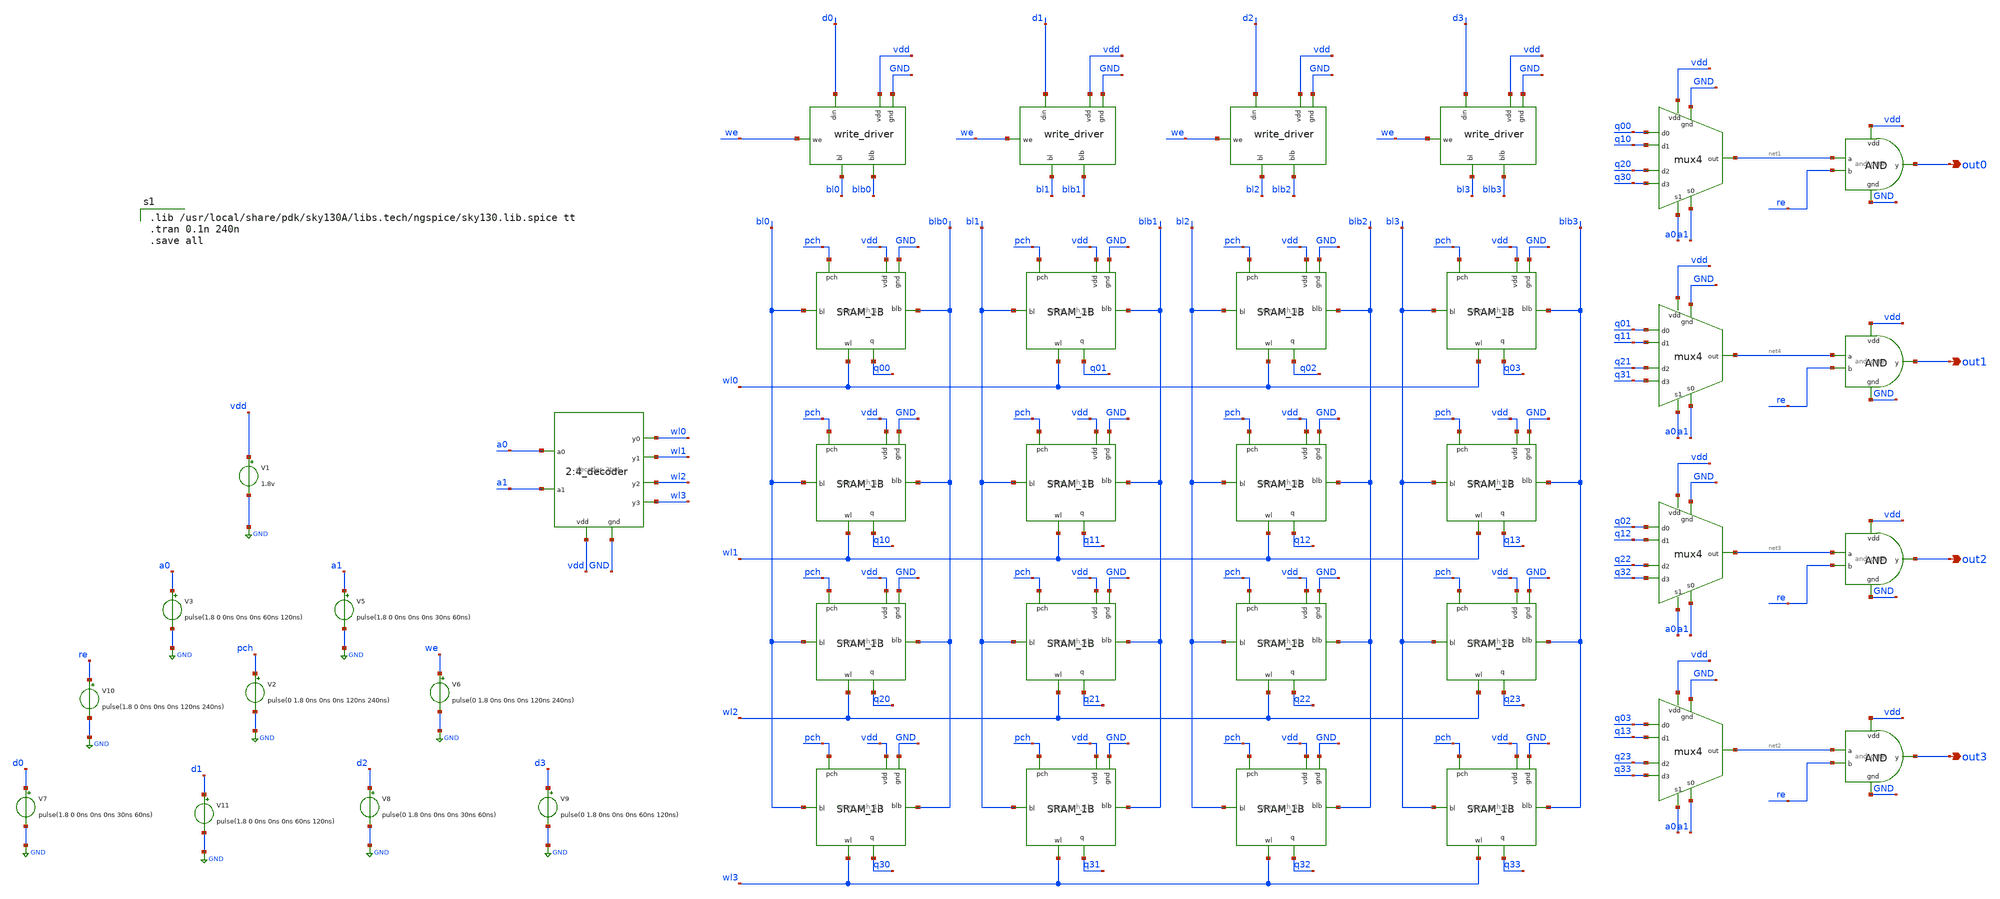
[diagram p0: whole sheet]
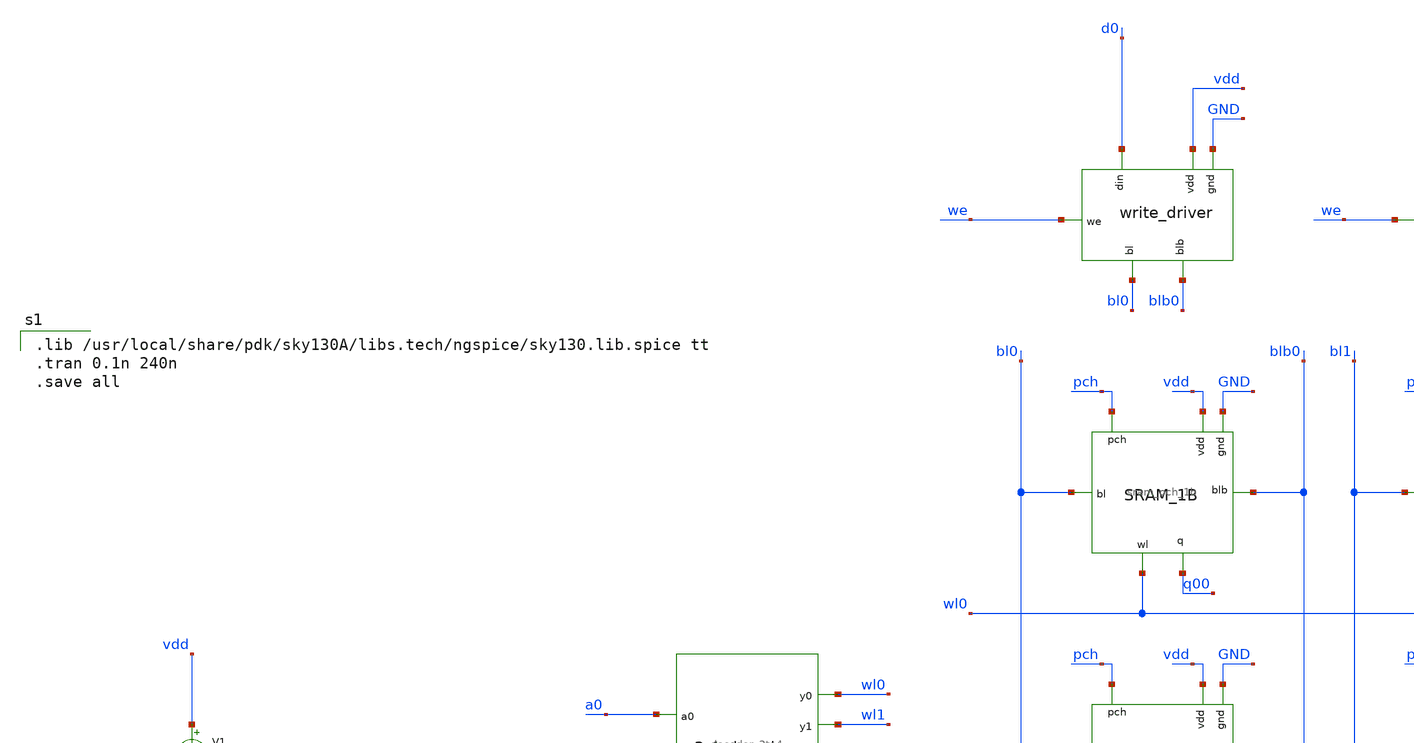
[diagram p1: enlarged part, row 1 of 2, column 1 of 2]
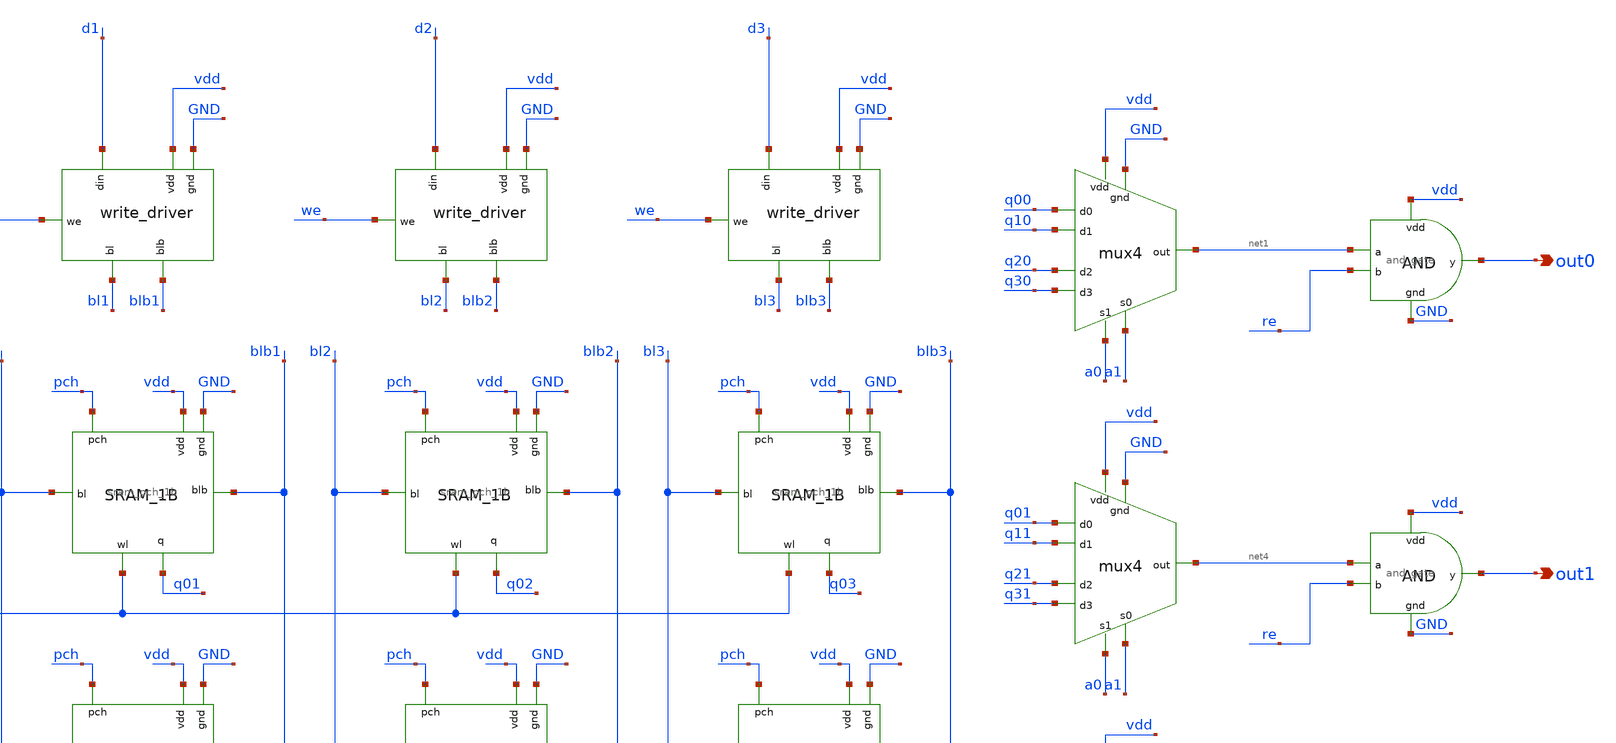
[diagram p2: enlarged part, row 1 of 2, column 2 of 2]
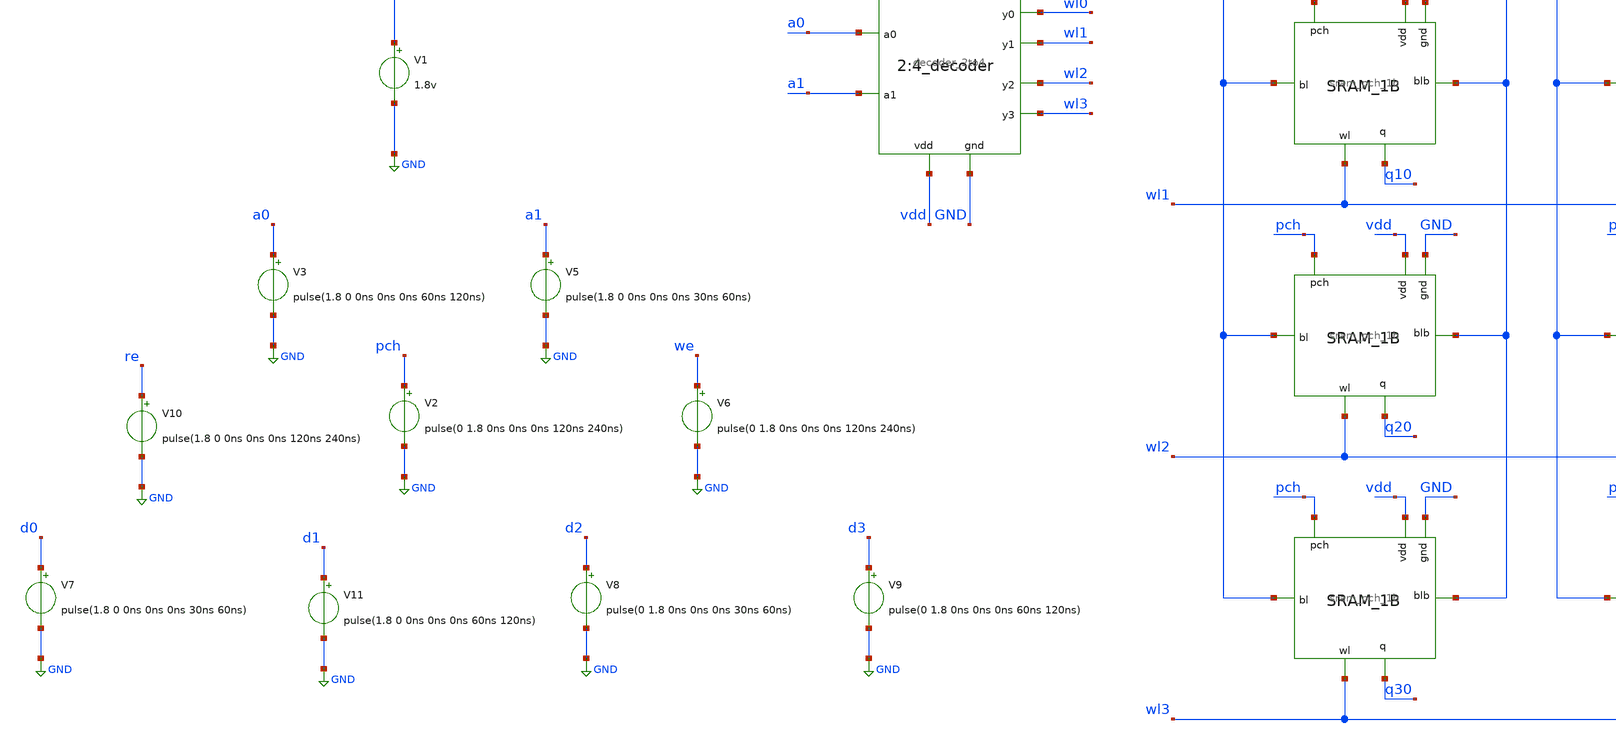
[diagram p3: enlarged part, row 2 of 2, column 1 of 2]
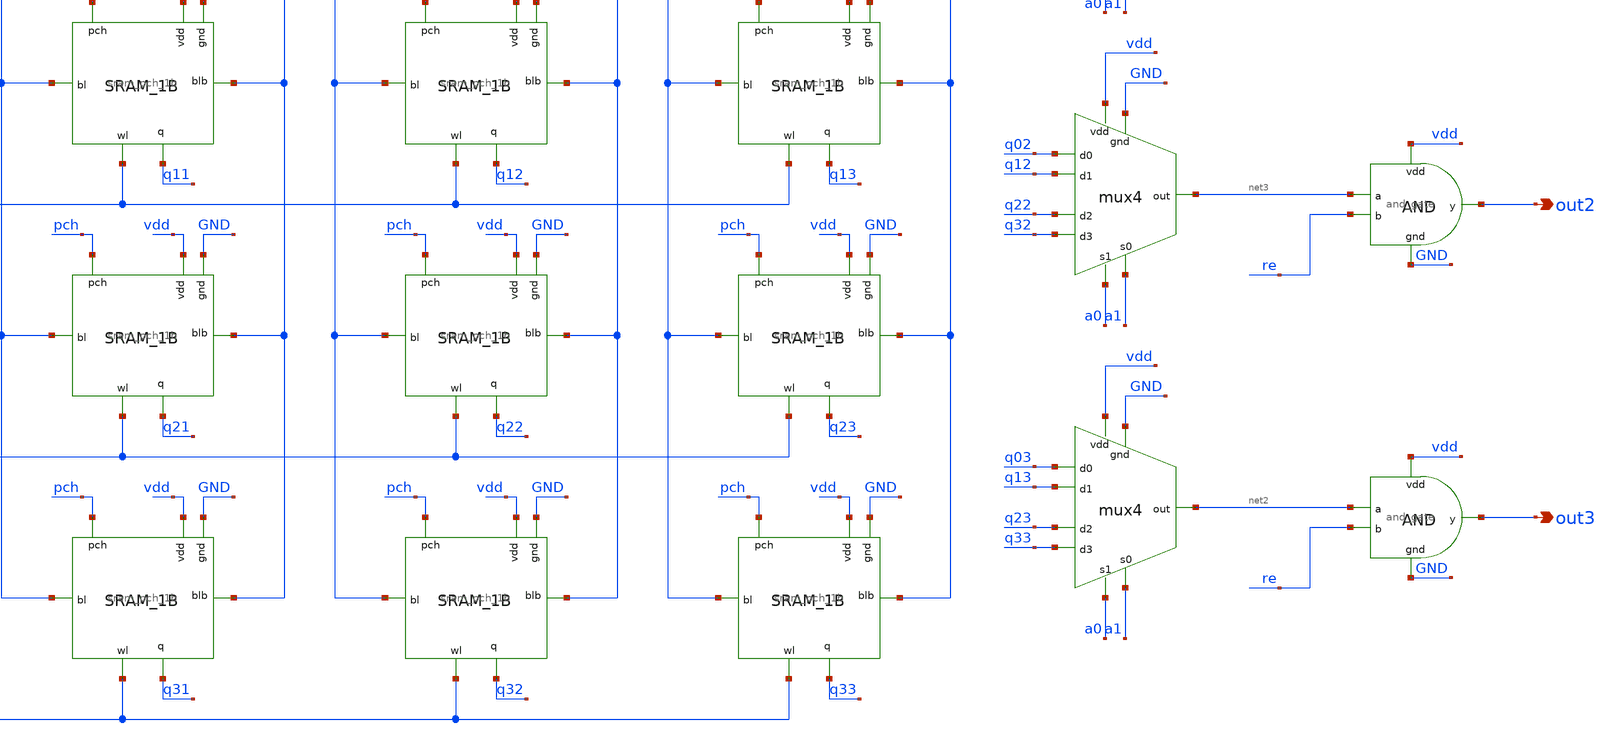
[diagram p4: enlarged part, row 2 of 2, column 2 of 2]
** sch_path: sram/4x4_sram_mux.sch
**.subckt 4x4_sram_mux out0 out1 out2 out3
*.opin out0
*.opin out1
*.opin out2
*.opin out3
x2 wl0 vdd GND a0 a1 wl1 wl2 wl3 decoder_2to4
x3 vdd GND d0 bl0 blb0 we write_driver
x21 vdd GND d1 bl1 blb1 we write_driver
x22 vdd GND d2 bl2 blb2 we write_driver
x23 vdd GND d3 bl3 blb3 we write_driver
V1 vdd GND 1.8v
V3 a0 GND pulse(1.8 0 0ns 0ns 0ns 60ns 120ns)
V2 pch GND pulse(0 1.8 0ns 0ns 0ns 120ns 240ns)
V5 a1 GND pulse(1.8 0 0ns 0ns 0ns 30ns 60ns)
V6 we GND pulse(0 1.8 0ns 0ns 0ns 120ns 240ns)
V7 d0 GND pulse(1.8 0 0ns 0ns 0ns 30ns 60ns)
V11 d1 GND pulse(1.8 0 0ns 0ns 0ns 60ns 120ns)
V8 d2 GND pulse(0 1.8 0ns 0ns 0ns 30ns 60ns)
V9 d3 GND pulse(0 1.8 0ns 0ns 0ns 60ns 120ns)
V10 re GND pulse(1.8 0 0ns 0ns 0ns 120ns 240ns)
x1 pch wl0 bl3 q03 GND vdd blb3 sram_pch_1b
x4 pch wl1 bl3 q13 GND vdd blb3 sram_pch_1b
x5 pch wl1 bl2 q12 GND vdd blb2 sram_pch_1b
x6 pch wl0 bl2 q02 GND vdd blb2 sram_pch_1b
x7 pch wl2 bl2 q22 GND vdd blb2 sram_pch_1b
x8 pch wl2 bl3 q23 GND vdd blb3 sram_pch_1b
x9 pch wl2 bl1 q21 GND vdd blb1 sram_pch_1b
x10 pch wl1 bl1 q11 GND vdd blb1 sram_pch_1b
x11 pch wl1 bl0 q10 GND vdd blb0 sram_pch_1b
x12 pch wl2 bl0 q20 GND vdd blb0 sram_pch_1b
x13 pch wl3 bl0 q30 GND vdd blb0 sram_pch_1b
x14 pch wl3 bl1 q31 GND vdd blb1 sram_pch_1b
x15 pch wl3 bl2 q32 GND vdd blb2 sram_pch_1b
x16 pch wl3 bl3 q33 GND vdd blb3 sram_pch_1b
x17 pch wl0 bl1 q01 GND vdd blb1 sram_pch_1b
x18 pch wl0 bl0 q00 GND vdd blb0 sram_pch_1b
x19 vdd GND q00 q10 net1 a0 q20 q30 a1 mux4
x20 vdd GND q01 q11 net4 a0 q21 q31 a1 mux4
x24 vdd GND q02 q12 net3 a0 q22 q32 a1 mux4
x25 vdd GND q03 q13 net2 a0 q23 q33 a1 mux4
x26 vdd net1 out0 re GND and_gate
x27 vdd net4 out1 re GND and_gate
x28 vdd net3 out2 re GND and_gate
x29 vdd net2 out3 re GND and_gate
**** begin user architecture code

.lib /usr/local/share/pdk/sky130A/libs.tech/ngspice/sky130.lib.spice tt
.tran 0.1n 240n
.save all

**** end user architecture code
**.ends

* expanding   symbol:  decoder_2to4.sym # of pins=8
** sym_path: sram/decoder_2to4.sym
** sch_path: sram/decoder_2to4.sch
.subckt decoder_2to4 y0 vdd gnd a0 a1 y1 y2 y3
*.opin y0
*.opin y1
*.opin y2
*.opin y3
*.ipin vdd
*.ipin gnd
*.ipin a0
*.ipin a1
x1 vdd a0b y0 a1b gnd and_gate
x2 vdd a0 a0b gnd inverter
x3 vdd a0b y1 a1 gnd and_gate
x4 vdd a0 y2 a1b gnd and_gate
x5 vdd a0 y3 a1 gnd and_gate
x6 vdd a1 a1b gnd inverter
.ends


* expanding   symbol:  write_driver.sym # of pins=6
** sym_path: sram/write_driver.sym
** sch_path: sram/write_driver.sch
.subckt write_driver vdd gnd din bl blb we
*.ipin din
*.ipin we
*.opin bl
*.opin blb
*.ipin vdd
*.ipin gnd
XM1 net2 web vdd vdd sky130_fd_pr__pfet_01v8 L=0.15 W=1 nf=1 ad='int((nf+1)/2) * W/nf * 0.29' as='int((nf+2)/2) * W/nf * 0.29'
+ pd='2*int((nf+1)/2) * (W/nf + 0.29)' ps='2*int((nf+2)/2) * (W/nf + 0.29)' nrd='0.29 / W' nrs='0.29 / W'
+ sa=0 sb=0 sd=0 mult=1 m=1
XM2 blb din net1 blb sky130_fd_pr__nfet_01v8 L=0.15 W=1 nf=1 ad='int((nf+1)/2) * W/nf * 0.29' as='int((nf+2)/2) * W/nf * 0.29'
+ pd='2*int((nf+1)/2) * (W/nf + 0.29)' ps='2*int((nf+2)/2) * (W/nf + 0.29)' nrd='0.29 / W' nrs='0.29 / W'
+ sa=0 sb=0 sd=0 mult=1 m=1
XM3 blb din net2 net2 sky130_fd_pr__pfet_01v8 L=0.15 W=1 nf=1 ad='int((nf+1)/2) * W/nf * 0.29' as='int((nf+2)/2) * W/nf * 0.29'
+ pd='2*int((nf+1)/2) * (W/nf + 0.29)' ps='2*int((nf+2)/2) * (W/nf + 0.29)' nrd='0.29 / W' nrs='0.29 / W'
+ sa=0 sb=0 sd=0 mult=1 m=1
XM4 net1 we gnd net1 sky130_fd_pr__nfet_01v8 L=0.15 W=1 nf=1 ad='int((nf+1)/2) * W/nf * 0.29' as='int((nf+2)/2) * W/nf * 0.29'
+ pd='2*int((nf+1)/2) * (W/nf + 0.29)' ps='2*int((nf+2)/2) * (W/nf + 0.29)' nrd='0.29 / W' nrs='0.29 / W'
+ sa=0 sb=0 sd=0 mult=1 m=1
XM5 net4 web vdd vdd sky130_fd_pr__pfet_01v8 L=0.15 W=1 nf=1 ad='int((nf+1)/2) * W/nf * 0.29' as='int((nf+2)/2) * W/nf * 0.29'
+ pd='2*int((nf+1)/2) * (W/nf + 0.29)' ps='2*int((nf+2)/2) * (W/nf + 0.29)' nrd='0.29 / W' nrs='0.29 / W'
+ sa=0 sb=0 sd=0 mult=1 m=1
XM6 bl dinb net3 net3 sky130_fd_pr__nfet_01v8 L=0.15 W=1 nf=1 ad='int((nf+1)/2) * W/nf * 0.29' as='int((nf+2)/2) * W/nf * 0.29'
+ pd='2*int((nf+1)/2) * (W/nf + 0.29)' ps='2*int((nf+2)/2) * (W/nf + 0.29)' nrd='0.29 / W' nrs='0.29 / W'
+ sa=0 sb=0 sd=0 mult=1 m=1
XM7 bl dinb net4 net4 sky130_fd_pr__pfet_01v8 L=0.15 W=1 nf=1 ad='int((nf+1)/2) * W/nf * 0.29' as='int((nf+2)/2) * W/nf * 0.29'
+ pd='2*int((nf+1)/2) * (W/nf + 0.29)' ps='2*int((nf+2)/2) * (W/nf + 0.29)' nrd='0.29 / W' nrs='0.29 / W'
+ sa=0 sb=0 sd=0 mult=1 m=1
XM8 net3 we gnd gnd sky130_fd_pr__nfet_01v8 L=0.15 W=1 nf=1 ad='int((nf+1)/2) * W/nf * 0.29' as='int((nf+2)/2) * W/nf * 0.29'
+ pd='2*int((nf+1)/2) * (W/nf + 0.29)' ps='2*int((nf+2)/2) * (W/nf + 0.29)' nrd='0.29 / W' nrs='0.29 / W'
+ sa=0 sb=0 sd=0 mult=1 m=1
x1 vdd din dinb gnd inverter
x2 vdd we web gnd inverter
.ends


* expanding   symbol:  sram_pch_1b.sym # of pins=7
** sym_path: sram/sram_pch_1b.sym
** sch_path: sram/sram_pch_1b.sch
.subckt sram_pch_1b pch wl bl q gnd vdd blb
*.ipin gnd
*.ipin bl
*.ipin blb
*.ipin vdd
*.ipin wl
*.ipin pch
*.opin q
XM1 blb wl net1 gnd sky130_fd_pr__nfet_01v8 L=0.15 W=1 nf=1 ad='int((nf+1)/2) * W/nf * 0.29' as='int((nf+2)/2) * W/nf * 0.29'
+ pd='2*int((nf+1)/2) * (W/nf + 0.29)' ps='2*int((nf+2)/2) * (W/nf + 0.29)' nrd='0.29 / W' nrs='0.29 / W'
+ sa=0 sb=0 sd=0 mult=1 m=1
XM3 q wl bl gnd sky130_fd_pr__nfet_01v8 L=0.15 W=1 nf=1 ad='int((nf+1)/2) * W/nf * 0.29' as='int((nf+2)/2) * W/nf * 0.29'
+ pd='2*int((nf+1)/2) * (W/nf + 0.29)' ps='2*int((nf+2)/2) * (W/nf + 0.29)' nrd='0.29 / W' nrs='0.29 / W'
+ sa=0 sb=0 sd=0 mult=1 m=1
XM5 q net1 vdd vdd sky130_fd_pr__pfet_01v8 L=0.15 W=1 nf=1 ad='int((nf+1)/2) * W/nf * 0.29' as='int((nf+2)/2) * W/nf * 0.29'
+ pd='2*int((nf+1)/2) * (W/nf + 0.29)' ps='2*int((nf+2)/2) * (W/nf + 0.29)' nrd='0.29 / W' nrs='0.29 / W'
+ sa=0 sb=0 sd=0 mult=1 m=1
XM6 net1 q vdd vdd sky130_fd_pr__pfet_01v8 L=0.15 W=1 nf=1 ad='int((nf+1)/2) * W/nf * 0.29' as='int((nf+2)/2) * W/nf * 0.29'
+ pd='2*int((nf+1)/2) * (W/nf + 0.29)' ps='2*int((nf+2)/2) * (W/nf + 0.29)' nrd='0.29 / W' nrs='0.29 / W'
+ sa=0 sb=0 sd=0 mult=1 m=1
XM7 bl pch vdd vdd sky130_fd_pr__pfet_01v8 L=0.15 W=1 nf=1 ad='int((nf+1)/2) * W/nf * 0.29' as='int((nf+2)/2) * W/nf * 0.29'
+ pd='2*int((nf+1)/2) * (W/nf + 0.29)' ps='2*int((nf+2)/2) * (W/nf + 0.29)' nrd='0.29 / W' nrs='0.29 / W'
+ sa=0 sb=0 sd=0 mult=1 m=1
XM8 blb pch vdd vdd sky130_fd_pr__pfet_01v8 L=0.15 W=1 nf=1 ad='int((nf+1)/2) * W/nf * 0.29' as='int((nf+2)/2) * W/nf * 0.29'
+ pd='2*int((nf+1)/2) * (W/nf + 0.29)' ps='2*int((nf+2)/2) * (W/nf + 0.29)' nrd='0.29 / W' nrs='0.29 / W'
+ sa=0 sb=0 sd=0 mult=1 m=1
XM9 bl pch blb blb sky130_fd_pr__pfet_01v8 L=0.15 W=1 nf=1 ad='int((nf+1)/2) * W/nf * 0.29' as='int((nf+2)/2) * W/nf * 0.29'
+ pd='2*int((nf+1)/2) * (W/nf + 0.29)' ps='2*int((nf+2)/2) * (W/nf + 0.29)' nrd='0.29 / W' nrs='0.29 / W'
+ sa=0 sb=0 sd=0 mult=1 m=1
XM2 net1 q gnd gnd sky130_fd_pr__nfet_01v8 L=0.15 W=1 nf=1 ad='int((nf+1)/2) * W/nf * 0.29' as='int((nf+2)/2) * W/nf * 0.29'
+ pd='2*int((nf+1)/2) * (W/nf + 0.29)' ps='2*int((nf+2)/2) * (W/nf + 0.29)' nrd='0.29 / W' nrs='0.29 / W'
+ sa=0 sb=0 sd=0 mult=1 m=1
XM4 q net1 gnd gnd sky130_fd_pr__nfet_01v8 L=0.15 W=1 nf=1 ad='int((nf+1)/2) * W/nf * 0.29' as='int((nf+2)/2) * W/nf * 0.29'
+ pd='2*int((nf+1)/2) * (W/nf + 0.29)' ps='2*int((nf+2)/2) * (W/nf + 0.29)' nrd='0.29 / W' nrs='0.29 / W'
+ sa=0 sb=0 sd=0 mult=1 m=1
.ends


* expanding   symbol:  mux4.sym # of pins=9
** sym_path: sram/mux4.sym
** sch_path: sram/mux4.sch
.subckt mux4 vdd gnd d0 d1 out s1 d2 d3 s0
*.ipin d0
*.ipin d1
*.ipin d2
*.ipin d3
*.ipin s0
*.ipin s1
*.opin out
*.ipin vdd
*.ipin gnd
x1 d0 s0 vdd gnd net1 d1 mux2_tg
x2 d2 s0 vdd gnd net2 d3 mux2_tg
x3 net1 s1 vdd gnd out net2 mux2_tg
.ends


* expanding   symbol:  and_gate.sym # of pins=5
** sym_path: sram/and_gate.sym
** sch_path: sram/and_gate.sch
.subckt and_gate vdd a y b gnd
*.ipin a
*.ipin b
*.ipin vdd
*.ipin gnd
*.opin y
x2 vdd net1 y gnd inverter
x1 vdd a b gnd net1 nand_gate
.ends


* expanding   symbol:  inverter.sym # of pins=4
** sym_path: sram/inverter.sym
** sch_path: sram/inverter.sch
.subckt inverter vdd vin vout gnd
*.ipin vin
*.ipin vdd
*.ipin gnd
*.opin vout
XM1 vout vin gnd gnd sky130_fd_pr__nfet_01v8 L=0.15 W=1 nf=1 ad='int((nf+1)/2) * W/nf * 0.29' as='int((nf+2)/2) * W/nf * 0.29'
+ pd='2*int((nf+1)/2) * (W/nf + 0.29)' ps='2*int((nf+2)/2) * (W/nf + 0.29)' nrd='0.29 / W' nrs='0.29 / W'
+ sa=0 sb=0 sd=0 mult=1 m=1
XM2 vout vin vdd vdd sky130_fd_pr__pfet_01v8 L=0.15 W=1 nf=1 ad='int((nf+1)/2) * W/nf * 0.29' as='int((nf+2)/2) * W/nf * 0.29'
+ pd='2*int((nf+1)/2) * (W/nf + 0.29)' ps='2*int((nf+2)/2) * (W/nf + 0.29)' nrd='0.29 / W' nrs='0.29 / W'
+ sa=0 sb=0 sd=0 mult=1 m=1
.ends


* expanding   symbol:  mux2_tg.sym # of pins=6
** sym_path: sram/mux2_tg.sym
** sch_path: sram/mux2_tg.sch
.subckt mux2_tg in0 c vdd gnd y in1
*.ipin in0
*.ipin in1
*.ipin c
*.opin y
*.ipin vdd
*.ipin gnd
XM5 y c in0 vdd sky130_fd_pr__pfet_01v8 L=0.15 W=1 nf=1 ad='int((nf+1)/2) * W/nf * 0.29' as='int((nf+2)/2) * W/nf * 0.29'
+ pd='2*int((nf+1)/2) * (W/nf + 0.29)' ps='2*int((nf+2)/2) * (W/nf + 0.29)' nrd='0.29 / W' nrs='0.29 / W'
+ sa=0 sb=0 sd=0 mult=1 m=1
XM2 in0 cb y gnd sky130_fd_pr__nfet_01v8 L=0.15 W=1 nf=1 ad='int((nf+1)/2) * W/nf * 0.29' as='int((nf+2)/2) * W/nf * 0.29'
+ pd='2*int((nf+1)/2) * (W/nf + 0.29)' ps='2*int((nf+2)/2) * (W/nf + 0.29)' nrd='0.29 / W' nrs='0.29 / W'
+ sa=0 sb=0 sd=0 mult=1 m=1
XM1 y cb in1 vdd sky130_fd_pr__pfet_01v8 L=0.15 W=1 nf=1 ad='int((nf+1)/2) * W/nf * 0.29' as='int((nf+2)/2) * W/nf * 0.29'
+ pd='2*int((nf+1)/2) * (W/nf + 0.29)' ps='2*int((nf+2)/2) * (W/nf + 0.29)' nrd='0.29 / W' nrs='0.29 / W'
+ sa=0 sb=0 sd=0 mult=1 m=1
XM3 in1 c y gnd sky130_fd_pr__nfet_01v8 L=0.15 W=1 nf=1 ad='int((nf+1)/2) * W/nf * 0.29' as='int((nf+2)/2) * W/nf * 0.29'
+ pd='2*int((nf+1)/2) * (W/nf + 0.29)' ps='2*int((nf+2)/2) * (W/nf + 0.29)' nrd='0.29 / W' nrs='0.29 / W'
+ sa=0 sb=0 sd=0 mult=1 m=1
x1 vdd c cb gnd inverter
.ends


* expanding   symbol:  nand_gate.sym # of pins=5
** sym_path: sram/nand_gate.sym
** sch_path: sram/nand_gate.sch
.subckt nand_gate vdd a b gnd y
*.ipin a
*.ipin b
*.ipin vdd
*.ipin gnd
*.opin y
XM1 y a vdd vdd sky130_fd_pr__pfet_01v8 L=0.15 W=1 nf=1 ad='int((nf+1)/2) * W/nf * 0.29' as='int((nf+2)/2) * W/nf * 0.29'
+ pd='2*int((nf+1)/2) * (W/nf + 0.29)' ps='2*int((nf+2)/2) * (W/nf + 0.29)' nrd='0.29 / W' nrs='0.29 / W'
+ sa=0 sb=0 sd=0 mult=1 m=1
XM2 y a net1 net1 sky130_fd_pr__nfet_01v8 L=0.15 W=1 nf=1 ad='int((nf+1)/2) * W/nf * 0.29' as='int((nf+2)/2) * W/nf * 0.29'
+ pd='2*int((nf+1)/2) * (W/nf + 0.29)' ps='2*int((nf+2)/2) * (W/nf + 0.29)' nrd='0.29 / W' nrs='0.29 / W'
+ sa=0 sb=0 sd=0 mult=1 m=1
XM3 y b vdd vdd sky130_fd_pr__pfet_01v8 L=0.15 W=1 nf=1 ad='int((nf+1)/2) * W/nf * 0.29' as='int((nf+2)/2) * W/nf * 0.29'
+ pd='2*int((nf+1)/2) * (W/nf + 0.29)' ps='2*int((nf+2)/2) * (W/nf + 0.29)' nrd='0.29 / W' nrs='0.29 / W'
+ sa=0 sb=0 sd=0 mult=1 m=1
XM4 net1 b gnd gnd sky130_fd_pr__nfet_01v8 L=0.15 W=1 nf=1 ad='int((nf+1)/2) * W/nf * 0.29' as='int((nf+2)/2) * W/nf * 0.29'
+ pd='2*int((nf+1)/2) * (W/nf + 0.29)' ps='2*int((nf+2)/2) * (W/nf + 0.29)' nrd='0.29 / W' nrs='0.29 / W'
+ sa=0 sb=0 sd=0 mult=1 m=1
.ends

.GLOBAL GND
.end
